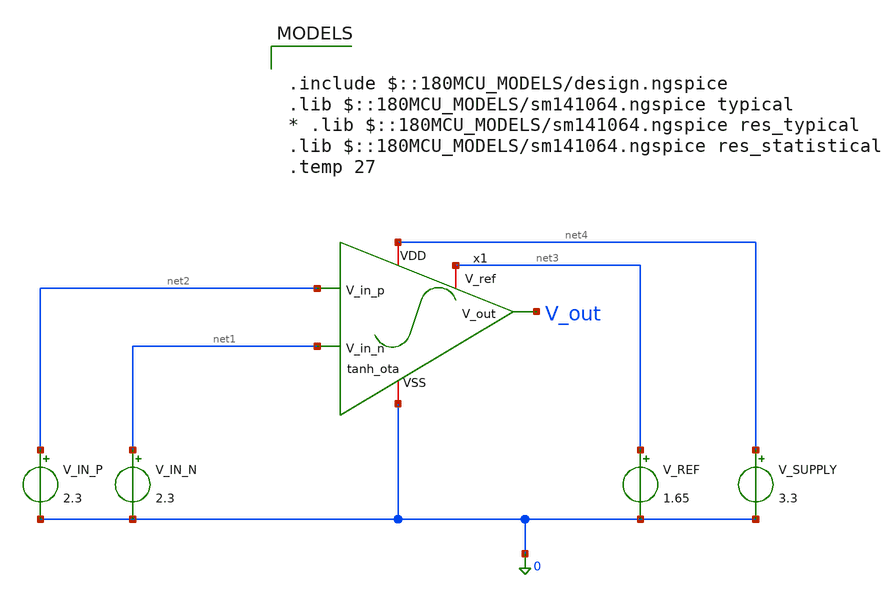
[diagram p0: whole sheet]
** sch_path: lvs/schematics/tb_tanh_ota.sch
**.subckt tb_tanh_ota
V_REF net3 0 1.65
V_SUPPLY net4 0 3.3
V_IN_N net1 0 2.3
V_IN_P net2 0 2.3
x1 net4 net3 V_out net2 net1 0 tanh_ota
**** begin user architecture code

.include $::180MCU_MODELS/design.ngspice
.lib $::180MCU_MODELS/sm141064.ngspice typical
* .lib $::180MCU_MODELS/sm141064.ngspice res_typical
.lib $::180MCU_MODELS/sm141064.ngspice res_statistical
.temp 27



.control
  op
  echo "--- tanh OTA x1: transistor op points ---"
  print @m.x1.xm1.m0[vgs] @m.x1.xm1.m0[vth] @m.x1.xm1.m0[vdsat] @m.x1.xm1.m0[id] @m.x1.xm1.m0[gm]
+ @m.x1.xm1.m0[gds]
  print @m.x1.xm2.m0[vgs] @m.x1.xm2.m0[vth] @m.x1.xm2.m0[vdsat] @m.x1.xm2.m0[id] @m.x1.xm2.m0[gm]
+ @m.x1.xm2.m0[gds]
  print @m.x1.xm3.m0[vgs] @m.x1.xm3.m0[vth] @m.x1.xm3.m0[vdsat] @m.x1.xm3.m0[id] @m.x1.xm3.m0[gm]
+ @m.x1.xm3.m0[gds]
  print @m.x1.xm4.m0[vgs] @m.x1.xm4.m0[vth] @m.x1.xm4.m0[vdsat] @m.x1.xm4.m0[id] @m.x1.xm4.m0[gm]
+ @m.x1.xm4.m0[gds]
  print @m.x1.xm5.m0[vgs] @m.x1.xm5.m0[vth] @m.x1.xm5.m0[vdsat] @m.x1.xm5.m0[id] @m.x1.xm5.m0[gm]
+ @m.x1.xm5.m0[gds]
  echo "--- tanh OTA x1: reference resistor ---"
  print @r.x1.xr1.rt1[resistance] @r.x1.xr1.rt2[resistance]
  dc V_IN_P 2.1 2.5 0.002
  let V_out = v(V_out)
  plot V_out title "tanh OTA: Saturating Transfer Characteristic"
  wrdata /foss/designs/analog-perceptron-gf180mcu/plots/tanh_ota_sweep.txt V_out
  * === OP-SWEEP DIAGNOSTIC: all 5 devices' headroom across full input range ===
  save all @m.x1.xm1.m0[vgs] @m.x1.xm1.m0[vth] @m.x1.xm1.m0[vdsat] @m.x1.xm1.m0[id] @m.x1.xm1.m0[gm] @m.x1.xm1.m0[gds] @m.x1.xm2.m0[vgs] @m.x1.xm2.m0[vth] @m.x1.xm2.m0[vdsat] @m.x1.xm2.m0[id] @m.x1.xm2.m0[gm] @m.x1.xm2.m0[gds] @m.x1.xm3.m0[vgs] @m.x1.xm3.m0[vth] @m.x1.xm3.m0[vdsat] @m.x1.xm3.m0[id] @m.x1.xm3.m0[gm] @m.x1.xm3.m0[gds] @m.x1.xm4.m0[vgs] @m.x1.xm4.m0[vth] @m.x1.xm4.m0[vdsat] @m.x1.xm4.m0[id] @m.x1.xm4.m0[gm] @m.x1.xm4.m0[gds] @m.x1.xm5.m0[vgs] @m.x1.xm5.m0[vth] @m.x1.xm5.m0[vdsat] @m.x1.xm5.m0[id] @m.x1.xm5.m0[gm] @m.x1.xm5.m0[gds]
  dc V_IN_P 2.1 2.5 0.002
  wrdata /foss/designs/analog-perceptron-gf180mcu/plots/opsweep_tanh_ota.txt v(V_out) @m.x1.xm1.m0[vgs] @m.x1.xm1.m0[vth] @m.x1.xm1.m0[vdsat] @m.x1.xm1.m0[id] @m.x1.xm1.m0[gm] @m.x1.xm1.m0[gds] @m.x1.xm2.m0[vgs] @m.x1.xm2.m0[vth] @m.x1.xm2.m0[vdsat] @m.x1.xm2.m0[id] @m.x1.xm2.m0[gm] @m.x1.xm2.m0[gds] @m.x1.xm3.m0[vgs] @m.x1.xm3.m0[vth] @m.x1.xm3.m0[vdsat] @m.x1.xm3.m0[id] @m.x1.xm3.m0[gm] @m.x1.xm3.m0[gds] @m.x1.xm4.m0[vgs] @m.x1.xm4.m0[vth] @m.x1.xm4.m0[vdsat] @m.x1.xm4.m0[id] @m.x1.xm4.m0[gm] @m.x1.xm4.m0[gds] @m.x1.xm5.m0[vgs] @m.x1.xm5.m0[vth] @m.x1.xm5.m0[vdsat] @m.x1.xm5.m0[id] @m.x1.xm5.m0[gm] @m.x1.xm5.m0[gds]
.endc


**** end user architecture code
**.ends
.end
